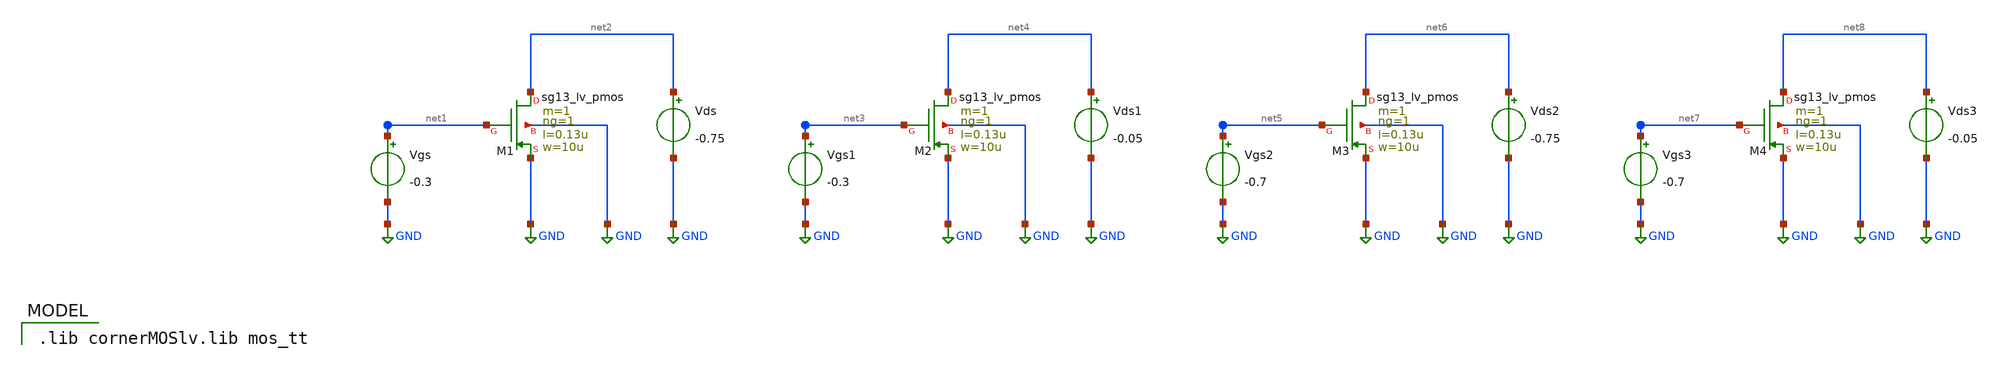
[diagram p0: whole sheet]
** sch_path: xschem/ex02.sch
* Copyright 2024 Harald Pretl, IIC@JKU
**.subckt ex02
Vgs net1 GND -0.3
Vds net2 GND -0.75
Vgs1 net3 GND -0.3
Vds1 net4 GND -0.05
Vgs2 net5 GND -0.7
Vds2 net6 GND -0.75
Vgs3 net7 GND -0.7
Vds3 net8 GND -0.05
XM1 net2 net1 GND GND sg13_lv_pmos w=10u l=0.13u ng=1 m=1 mm_ok=1
XM2 net4 net3 GND GND sg13_lv_pmos w=10u l=0.13u ng=1 m=1 mm_ok=1
XM3 net6 net5 GND GND sg13_lv_pmos w=10u l=0.13u ng=1 m=1 mm_ok=1
XM4 net8 net7 GND GND sg13_lv_pmos w=10u l=0.13u ng=1 m=1 mm_ok=1
**** begin user architecture code
 .lib cornerMOSlv.lib mos_tt



.temp 27
.control
save all

save @n.xm1.nsg13_lv_pmos[ids]
save @n.xm1.nsg13_lv_pmos[gm]
save @n.xm1.nsg13_lv_pmos[gmb]
save @n.xm1.nsg13_lv_pmos[gds]
save @n.xm1.nsg13_lv_pmos[cgg]
save @n.xm1.nsg13_lv_pmos[cgd]
save @n.xm1.nsg13_lv_pmos[cgs]
save @n.xm1.nsg13_lv_pmos[cgb]
save @n.xm1.nsg13_lv_pmos[fug]
save @n.xm1.nsg13_lv_pmos[sid]

save @n.xm2.nsg13_lv_pmos[ids]
save @n.xm2.nsg13_lv_pmos[gm]
save @n.xm2.nsg13_lv_pmos[gmb]
save @n.xm2.nsg13_lv_pmos[gds]
save @n.xm2.nsg13_lv_pmos[cgg]
save @n.xm2.nsg13_lv_pmos[cgd]
save @n.xm2.nsg13_lv_pmos[cgs]
save @n.xm2.nsg13_lv_pmos[cgb]
save @n.xm2.nsg13_lv_pmos[fug]
save @n.xm2.nsg13_lv_pmos[sid]

save @n.xm3.nsg13_lv_pmos[ids]
save @n.xm3.nsg13_lv_pmos[gm]
save @n.xm3.nsg13_lv_pmos[gmb]
save @n.xm3.nsg13_lv_pmos[gds]
save @n.xm3.nsg13_lv_pmos[cgg]
save @n.xm3.nsg13_lv_pmos[cgd]
save @n.xm3.nsg13_lv_pmos[cgs]
save @n.xm3.nsg13_lv_pmos[cgb]
save @n.xm3.nsg13_lv_pmos[fug]
save @n.xm3.nsg13_lv_pmos[sid]

save @n.xm4.nsg13_lv_pmos[ids]
save @n.xm4.nsg13_lv_pmos[gm]
save @n.xm4.nsg13_lv_pmos[gmb]
save @n.xm4.nsg13_lv_pmos[gds]
save @n.xm4.nsg13_lv_pmos[cgg]
save @n.xm4.nsg13_lv_pmos[cgd]
save @n.xm4.nsg13_lv_pmos[cgs]
save @n.xm4.nsg13_lv_pmos[cgb]
save @n.xm4.nsg13_lv_pmos[fug]
save @n.xm4.nsg13_lv_pmos[sid]

op
write ex02.raw
.endc


**** end user architecture code
**.ends
.GLOBAL GND
.end
